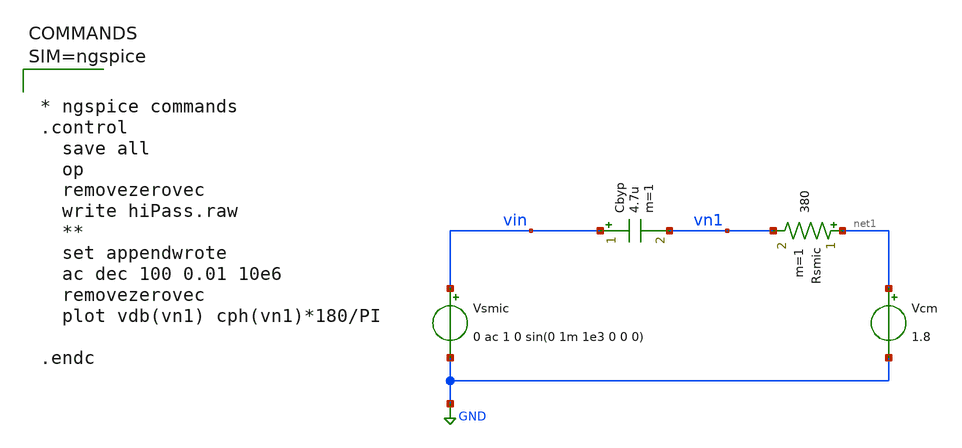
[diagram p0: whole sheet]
** sch_path: xschem/hipass.sch
**.subckt hipass
Vsmic vin GND 0 ac 1 0 sin(0 1m 1e3 0 0 0)
Rsmic net1 vn1 380 m=1
Cbyp vin vn1 4.7u m=1
Vcm net1 GND 1.8
**** begin user architecture code



* ngspice commands
.control
  save all
  op
  removezerovec
  write hiPass.raw
  **
  set appendwrote
  ac dec 100 0.01 10e6
  removezerovec
  plot vdb(vn1) cph(vn1)*180/PI

.endc



**** end user architecture code
**.ends
.GLOBAL GND
.end
